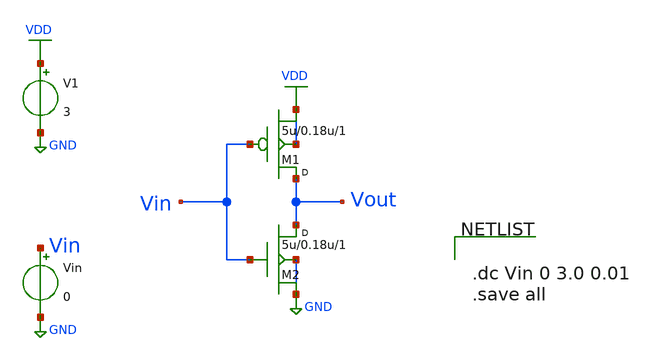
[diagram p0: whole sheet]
** sch_path: designs/0_inverter/inverter.sch
**.subckt inverter
V1 VDD GND 3
Vin Vin GND 0
M1 Vout Vin VDD VDD pmos w=5u l=0.18u m=1
M2 Vout Vin GND GND nmos w=5u l=0.18u m=1
**** begin user architecture code


.dc Vin 0 3.0 0.01
.save all



.model nmos NMOS (VTO=0.7 KP=200u L=0.18u W=5u)
.model pmos PMOS (VTO=-0.7 KP=100u L=0.18u W=5u)


**** end user architecture code
**.ends
.GLOBAL VDD
.GLOBAL GND
.end
